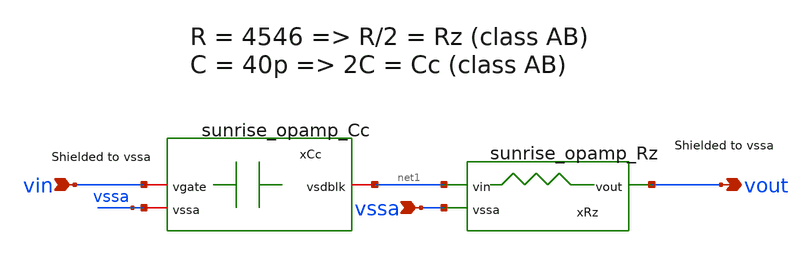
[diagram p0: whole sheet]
** sch_path: Schematics_Layout/sunrise_opamp_ncomp/sunrise_opamp_ncomp.sch
**.subckt sunrise_opamp_ncomp vssa vout vin
*.ipin vssa
*.opin vout
*.ipin vin
xCc vin net1 vssa sunrise_opamp_Cc
xRz vssa vout net1 sunrise_opamp_Rz
**.ends
.end
